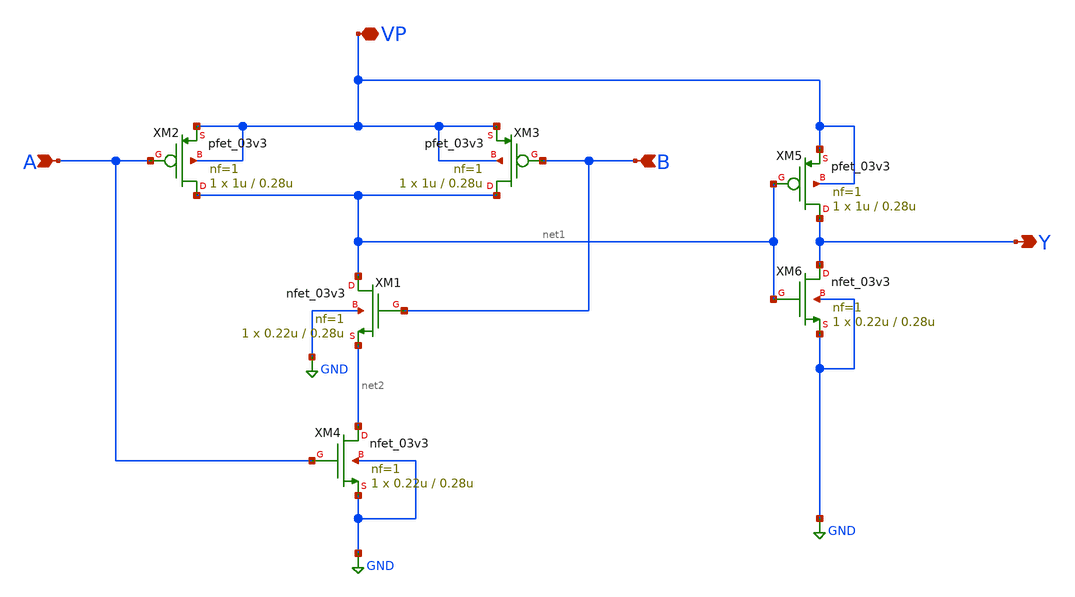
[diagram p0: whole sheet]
** sch_path: AND2.sch
**.subckt AND2 A B Y VP
*.ipin A
*.ipin B
*.opin Y
*.iopin VP
XM1 net1 B net2 GND nfet_03v3 L=0.28u W=0.22u nf=1 ad='int((nf+1)/2) * W/nf * 0.18u' as='int((nf+2)/2) * W/nf * 0.18u'
+ pd='2*int((nf+1)/2) * (W/nf + 0.18u)' ps='2*int((nf+2)/2) * (W/nf + 0.18u)' nrd='0.18u / W' nrs='0.18u / W'
+ sa=0 sb=0 sd=0 m=1
XM2 net1 A VP VP pfet_03v3 L=0.28u W=1u nf=1 ad='int((nf+1)/2) * W/nf * 0.18u' as='int((nf+2)/2) * W/nf * 0.18u'
+ pd='2*int((nf+1)/2) * (W/nf + 0.18u)' ps='2*int((nf+2)/2) * (W/nf + 0.18u)' nrd='0.18u / W' nrs='0.18u / W'
+ sa=0 sb=0 sd=0 m=1
XM4 net2 A GND GND nfet_03v3 L=0.28u W=0.22u nf=1 ad='int((nf+1)/2) * W/nf * 0.18u' as='int((nf+2)/2) * W/nf * 0.18u'
+ pd='2*int((nf+1)/2) * (W/nf + 0.18u)' ps='2*int((nf+2)/2) * (W/nf + 0.18u)' nrd='0.18u / W' nrs='0.18u / W'
+ sa=0 sb=0 sd=0 m=1
XM5 Y net1 VP VP pfet_03v3 L=0.28u W=1u nf=1 ad='int((nf+1)/2) * W/nf * 0.18u' as='int((nf+2)/2) * W/nf * 0.18u'
+ pd='2*int((nf+1)/2) * (W/nf + 0.18u)' ps='2*int((nf+2)/2) * (W/nf + 0.18u)' nrd='0.18u / W' nrs='0.18u / W'
+ sa=0 sb=0 sd=0 m=1
XM6 Y net1 GND GND nfet_03v3 L=0.28u W=0.22u nf=1 ad='int((nf+1)/2) * W/nf * 0.18u' as='int((nf+2)/2) * W/nf * 0.18u'
+ pd='2*int((nf+1)/2) * (W/nf + 0.18u)' ps='2*int((nf+2)/2) * (W/nf + 0.18u)' nrd='0.18u / W' nrs='0.18u / W'
+ sa=0 sb=0 sd=0 m=1
XM3 net1 B VP VP pfet_03v3 L=0.28u W=1u nf=1 ad='int((nf+1)/2) * W/nf * 0.18u' as='int((nf+2)/2) * W/nf * 0.18u'
+ pd='2*int((nf+1)/2) * (W/nf + 0.18u)' ps='2*int((nf+2)/2) * (W/nf + 0.18u)' nrd='0.18u / W' nrs='0.18u / W'
+ sa=0 sb=0 sd=0 m=1
**.ends
.GLOBAL GND
.end
